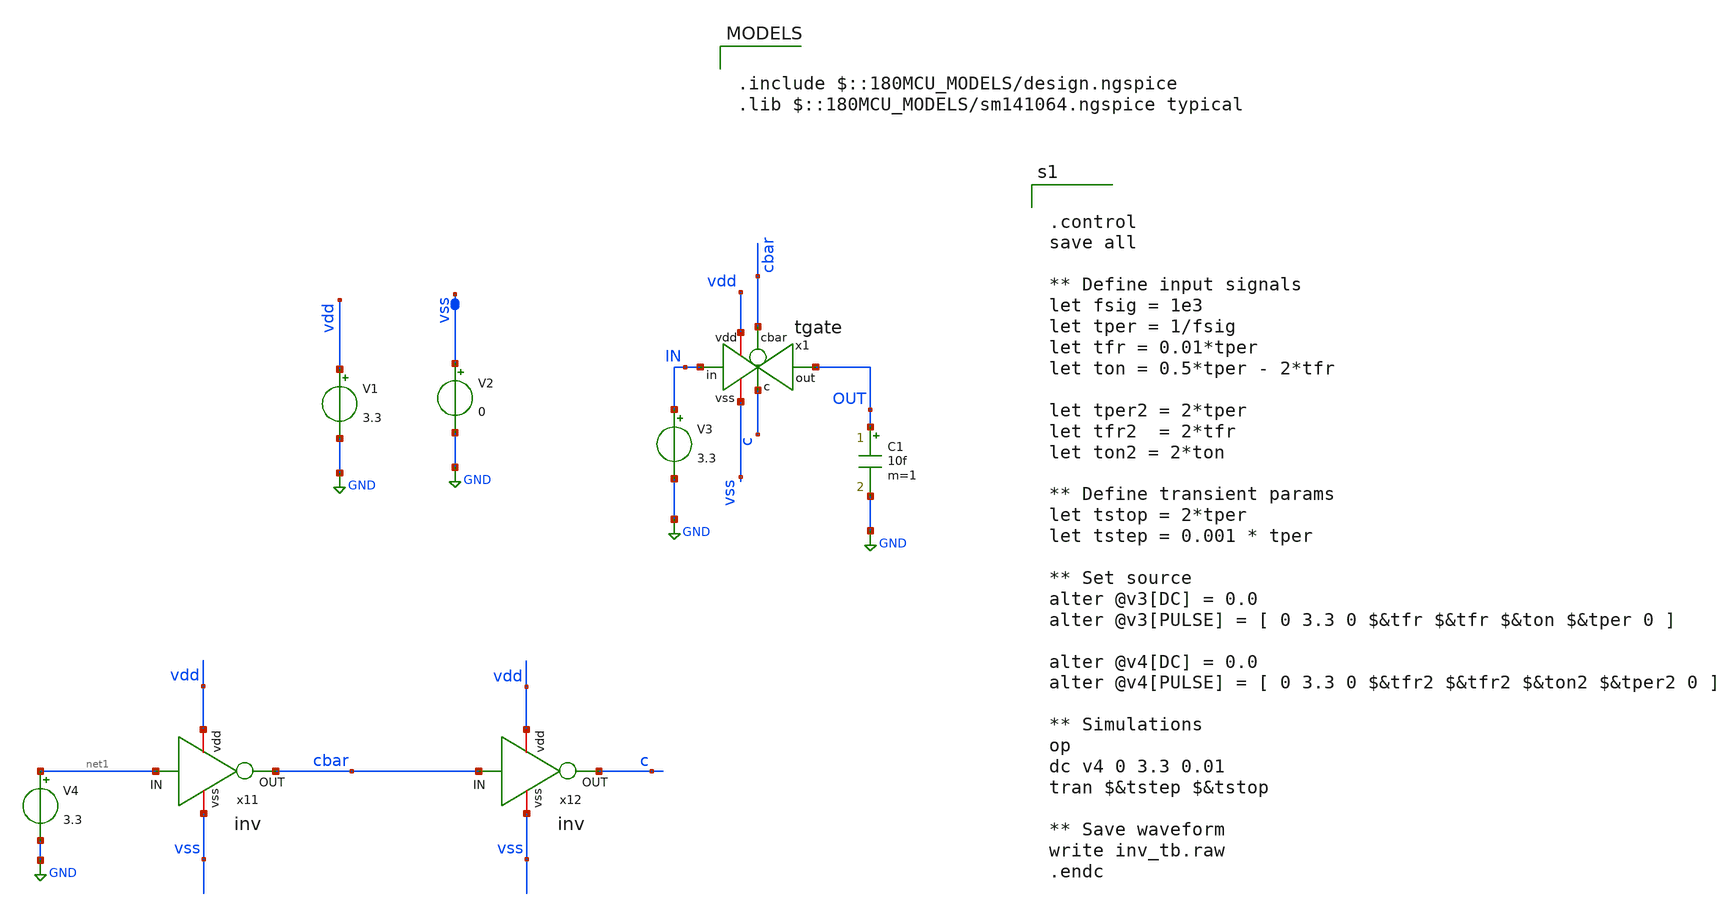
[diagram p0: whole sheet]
** sch_path: tgate_tb.sch
**.subckt tgate_tb
V1 vdd GND 3.3
V2 vss GND 0
V3 IN GND 3.3
C1 OUT GND 10f m=1
x1 IN vdd cbar c vss OUT tgate
x11 vdd net1 cbar vss inv
x12 vdd cbar c vss inv
V4 net1 GND 3.3
**** begin user architecture code

.include $::180MCU_MODELS/design.ngspice
.lib $::180MCU_MODELS/sm141064.ngspice typical



.control
save all

** Define input signals
let fsig = 1e3
let tper = 1/fsig
let tfr = 0.01*tper
let ton = 0.5*tper - 2*tfr

let tper2 = 2*tper
let tfr2  = 2*tfr
let ton2 = 2*ton

** Define transient params
let tstop = 2*tper
let tstep = 0.001 * tper

** Set source
alter @v3[DC] = 0.0
alter @v3[PULSE] = [ 0 3.3 0 $&tfr $&tfr $&ton $&tper 0 ]

alter @v4[DC] = 0.0
alter @v4[PULSE] = [ 0 3.3 0 $&tfr2 $&tfr2 $&ton2 $&tper2 0 ]

** Simulations
op
dc v4 0 3.3 0.01
tran $&tstep $&tstop

** Save waveform
write inv_tb.raw
.endc


**** end user architecture code
**.ends

* expanding   symbol:  tgate.sym # of pins=6
** sym_path: tgate.sym
** sch_path: tgate.sch
.subckt tgate in vdd cbar c vss out
*.ipin in
*.opin out
*.ipin cbar
*.ipin c
*.iopin vdd
*.iopin vss
XM1 out cbar in vdd pfet_03v3 L=0.28u W=1u nf=1 ad='int((nf+1)/2) * W/nf * 0.18u' as='int((nf+2)/2) * W/nf * 0.18u'
+ pd='2*int((nf+1)/2) * (W/nf + 0.18u)' ps='2*int((nf+2)/2) * (W/nf + 0.18u)' nrd='0.18u / W' nrs='0.18u / W'
+ sa=0 sb=0 sd=0 m=1
XM2 out c in vss nfet_03v3 L=0.28u W=1u nf=1 ad='int((nf+1)/2) * W/nf * 0.18u' as='int((nf+2)/2) * W/nf * 0.18u'
+ pd='2*int((nf+1)/2) * (W/nf + 0.18u)' ps='2*int((nf+2)/2) * (W/nf + 0.18u)' nrd='0.18u / W' nrs='0.18u / W'
+ sa=0 sb=0 sd=0 m=1
.ends


* expanding   symbol:  inv.sym # of pins=4
** sym_path: inv.sym
** sch_path: inv.sch
.subckt inv vdd IN OUT vss
*.ipin IN
*.opin OUT
*.iopin vdd
*.iopin vss
XM1 OUT IN vss vss nfet_03v3 L=0.28u W=1u nf=1 ad='int((nf+1)/2) * W/nf * 0.18u' as='int((nf+2)/2) * W/nf * 0.18u'
+ pd='2*int((nf+1)/2) * (W/nf + 0.18u)' ps='2*int((nf+2)/2) * (W/nf + 0.18u)' nrd='0.18u / W' nrs='0.18u / W'
+ sa=0 sb=0 sd=0 m=1
XM2 OUT IN vdd vdd pfet_03v3 L=0.28u W=1u nf=1 ad='int((nf+1)/2) * W/nf * 0.18u' as='int((nf+2)/2) * W/nf * 0.18u'
+ pd='2*int((nf+1)/2) * (W/nf + 0.18u)' ps='2*int((nf+2)/2) * (W/nf + 0.18u)' nrd='0.18u / W' nrs='0.18u / W'
+ sa=0 sb=0 sd=0 m=1
.ends

.GLOBAL GND
.end
